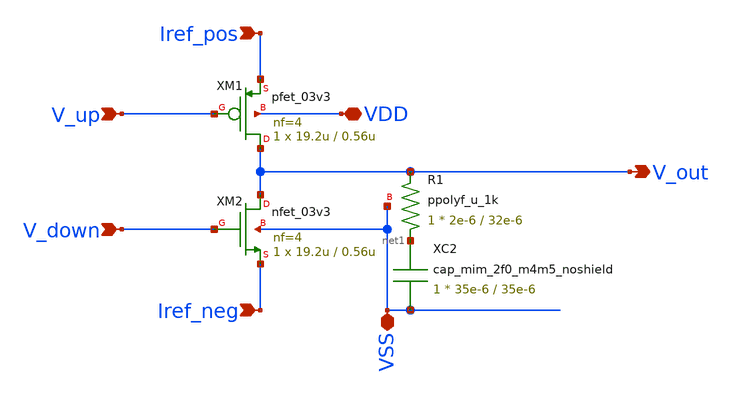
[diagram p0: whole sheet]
** sch_path: rha-vga-pll-blocks/blocks/pll/cpump.sch
**.subckt cpump Iref_pos Iref_neg V_up V_down VDD VSS V_out
*.ipin Iref_pos
*.ipin Iref_neg
*.ipin V_up
*.ipin V_down
*.iopin VDD
*.iopin VSS
*.opin V_out
XM2 V_out V_down Iref_neg VSS nfet_03v3 L=0.56u W=19.2u nf=4 ad='int((nf+1)/2) * W/nf * 0.18u' as='int((nf+2)/2) * W/nf * 0.18u'
+ pd='2*int((nf+1)/2) * (W/nf + 0.18u)' ps='2*int((nf+2)/2) * (W/nf + 0.18u)' nrd='0.18u / W' nrs='0.18u / W'
+ sa=0 sb=0 sd=0 m=1
XR1 net1 V_out VSS ppolyf_u_1k r_width=2e-6 r_length=32e-6 m=1
XM1 V_out V_up Iref_pos VDD pfet_03v3 L=0.56u W=19.2u nf=4 ad='int((nf+1)/2) * W/nf * 0.18u' as='int((nf+2)/2) * W/nf * 0.18u'
+ pd='2*int((nf+1)/2) * (W/nf + 0.18u)' ps='2*int((nf+2)/2) * (W/nf + 0.18u)' nrd='0.18u / W' nrs='0.18u / W'
+ sa=0 sb=0 sd=0 m=1
XC2 net1 VSS cap_mim_2f0_m4m5_noshield c_width=35e-6 c_length=35e-6 m=1
**.ends
.end
